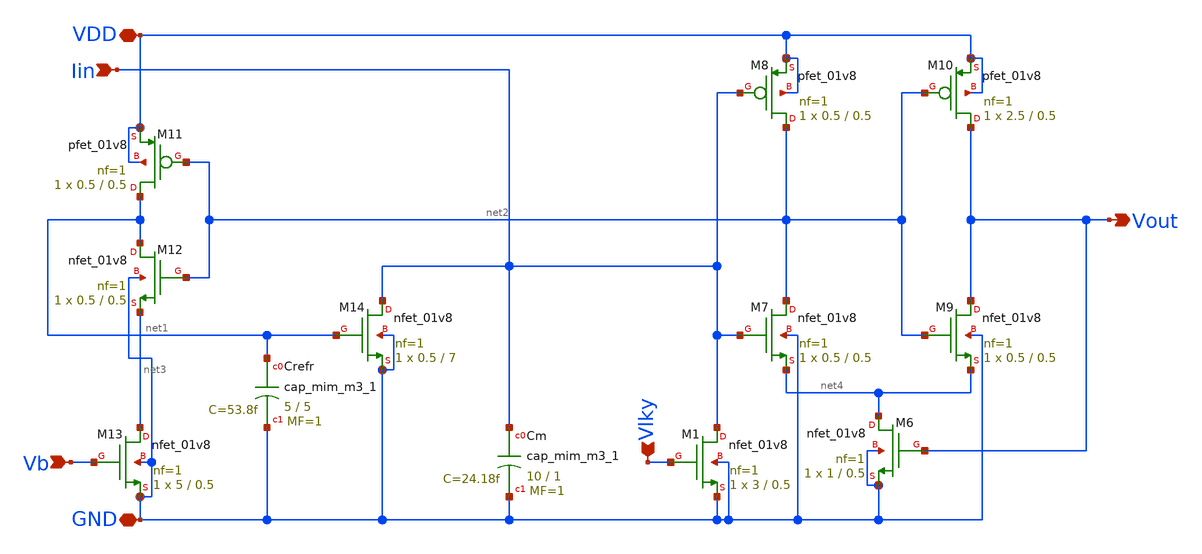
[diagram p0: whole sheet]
** sch_path: LIF_neuron/Input_Layer_LIF.sch
**.subckt Input_Layer_LIF GND Vb VDD Vout Iin Vlky
*.iopin GND
*.ipin Vb
*.iopin VDD
*.opin Vout
*.ipin Iin
*.ipin Vlky
XM13 net3 Vb GND GND sky130_fd_pr__nfet_01v8 L=0.5 W=5 nf=1 ad='int((nf+1)/2) * W/nf * 0.29' as='int((nf+2)/2) * W/nf * 0.29'
+ pd='2*int((nf+1)/2) * (W/nf + 0.29)' ps='2*int((nf+2)/2) * (W/nf + 0.29)' nrd='0.29 / W' nrs='0.29 / W'
+ sa=0 sb=0 sd=0 mult=1 m=1
XM12 net1 net2 net3 GND sky130_fd_pr__nfet_01v8 L=0.5 W=0.5 nf=1 ad='int((nf+1)/2) * W/nf * 0.29' as='int((nf+2)/2) * W/nf * 0.29'
+ pd='2*int((nf+1)/2) * (W/nf + 0.29)' ps='2*int((nf+2)/2) * (W/nf + 0.29)' nrd='0.29 / W' nrs='0.29 / W'
+ sa=0 sb=0 sd=0 mult=1 m=1
XM11 net1 net2 VDD VDD sky130_fd_pr__pfet_01v8 L=0.5 W=0.5 nf=1 ad='int((nf+1)/2) * W/nf * 0.29' as='int((nf+2)/2) * W/nf * 0.29'
+ pd='2*int((nf+1)/2) * (W/nf + 0.29)' ps='2*int((nf+2)/2) * (W/nf + 0.29)' nrd='0.29 / W' nrs='0.29 / W'
+ sa=0 sb=0 sd=0 mult=1 m=1
XCrefr net1 GND sky130_fd_pr__cap_mim_m3_1 W=5 L=5 MF=1 m=1
XM14 Iin net1 GND GND sky130_fd_pr__nfet_01v8 L=7 W=0.5 nf=1 ad='int((nf+1)/2) * W/nf * 0.29' as='int((nf+2)/2) * W/nf * 0.29'
+ pd='2*int((nf+1)/2) * (W/nf + 0.29)' ps='2*int((nf+2)/2) * (W/nf + 0.29)' nrd='0.29 / W' nrs='0.29 / W'
+ sa=0 sb=0 sd=0 mult=1 m=1
XCm Iin GND sky130_fd_pr__cap_mim_m3_1 W=10 L=1 MF=1 m=1
XM6 net4 Vout GND GND sky130_fd_pr__nfet_01v8 L=0.5 W=1 nf=1 ad='int((nf+1)/2) * W/nf * 0.29' as='int((nf+2)/2) * W/nf * 0.29'
+ pd='2*int((nf+1)/2) * (W/nf + 0.29)' ps='2*int((nf+2)/2) * (W/nf + 0.29)' nrd='0.29 / W' nrs='0.29 / W'
+ sa=0 sb=0 sd=0 mult=1 m=1
XM7 net2 Iin net4 GND sky130_fd_pr__nfet_01v8 L=0.5 W=0.5 nf=1 ad='int((nf+1)/2) * W/nf * 0.29' as='int((nf+2)/2) * W/nf * 0.29'
+ pd='2*int((nf+1)/2) * (W/nf + 0.29)' ps='2*int((nf+2)/2) * (W/nf + 0.29)' nrd='0.29 / W' nrs='0.29 / W'
+ sa=0 sb=0 sd=0 mult=1 m=1
XM8 net2 Iin VDD VDD sky130_fd_pr__pfet_01v8 L=0.5 W=0.5 nf=1 ad='int((nf+1)/2) * W/nf * 0.29' as='int((nf+2)/2) * W/nf * 0.29'
+ pd='2*int((nf+1)/2) * (W/nf + 0.29)' ps='2*int((nf+2)/2) * (W/nf + 0.29)' nrd='0.29 / W' nrs='0.29 / W'
+ sa=0 sb=0 sd=0 mult=1 m=1
XM9 Vout net2 net4 GND sky130_fd_pr__nfet_01v8 L=0.5 W=0.5 nf=1 ad='int((nf+1)/2) * W/nf * 0.29' as='int((nf+2)/2) * W/nf * 0.29'
+ pd='2*int((nf+1)/2) * (W/nf + 0.29)' ps='2*int((nf+2)/2) * (W/nf + 0.29)' nrd='0.29 / W' nrs='0.29 / W'
+ sa=0 sb=0 sd=0 mult=1 m=1
XM10 Vout net2 VDD VDD sky130_fd_pr__pfet_01v8 L=0.5 W=2.5 nf=1 ad='int((nf+1)/2) * W/nf * 0.29' as='int((nf+2)/2) * W/nf * 0.29'
+ pd='2*int((nf+1)/2) * (W/nf + 0.29)' ps='2*int((nf+2)/2) * (W/nf + 0.29)' nrd='0.29 / W' nrs='0.29 / W'
+ sa=0 sb=0 sd=0 mult=1 m=1
XM1 Iin Vlky GND GND sky130_fd_pr__nfet_01v8 L=0.5 W=3 nf=1 ad='int((nf+1)/2) * W/nf * 0.29' as='int((nf+2)/2) * W/nf * 0.29'
+ pd='2*int((nf+1)/2) * (W/nf + 0.29)' ps='2*int((nf+2)/2) * (W/nf + 0.29)' nrd='0.29 / W' nrs='0.29 / W'
+ sa=0 sb=0 sd=0 mult=1 m=1
**.ends
.end
